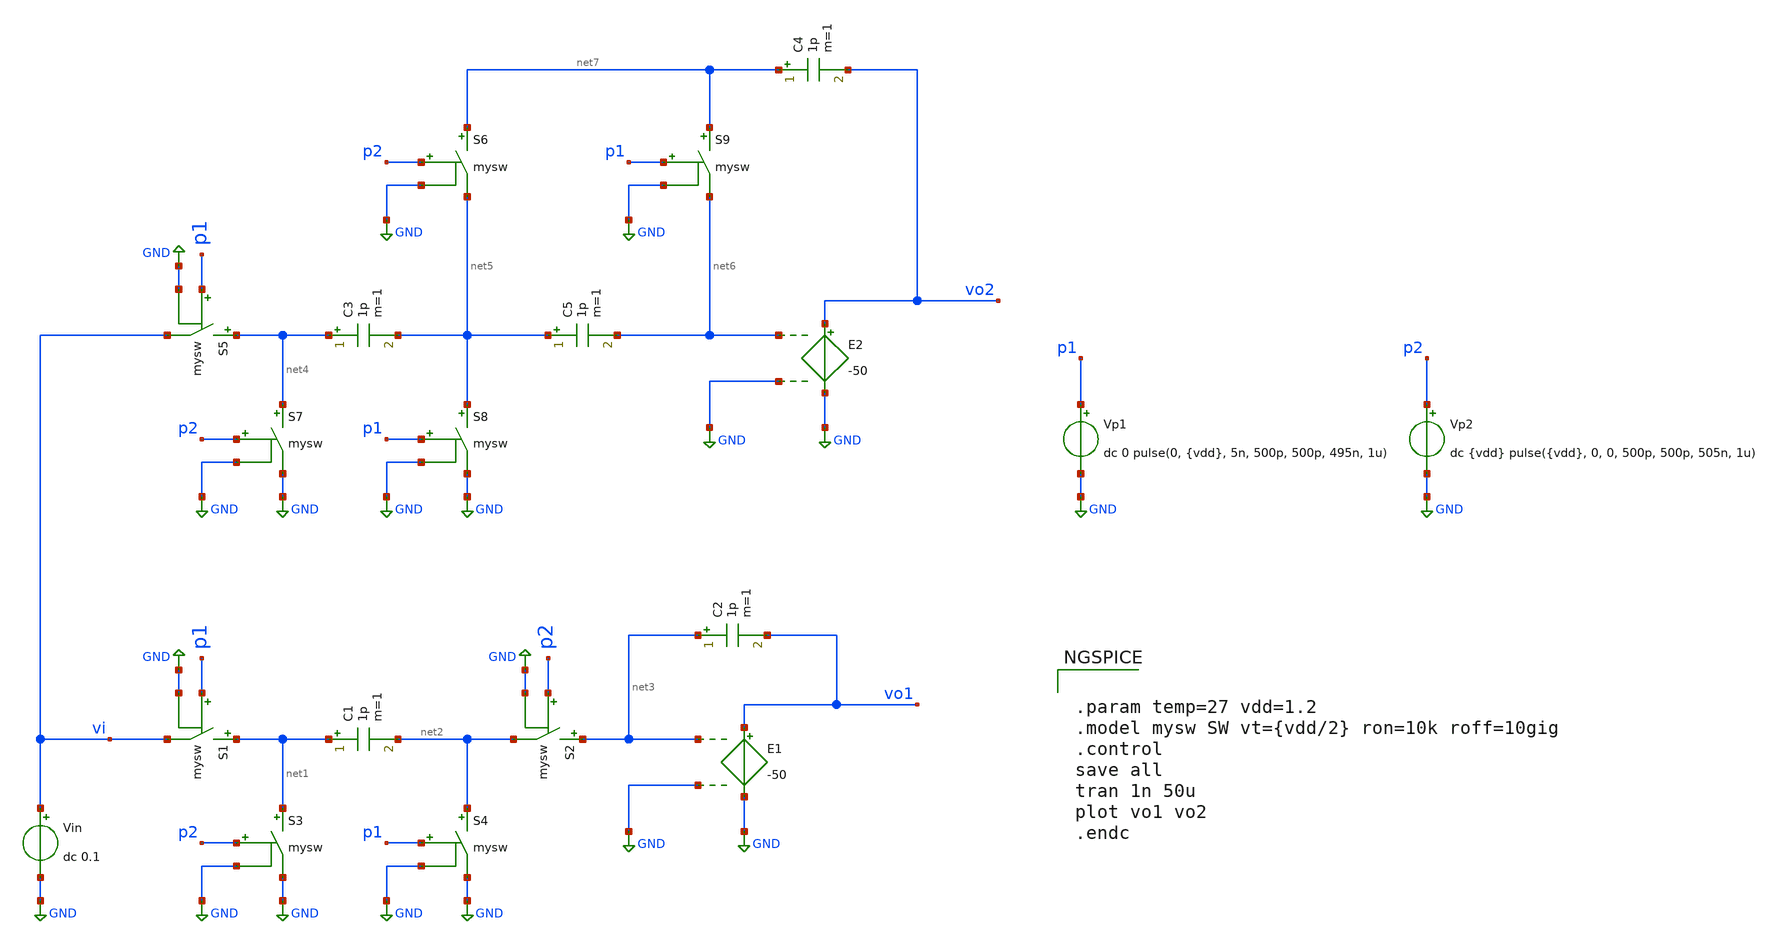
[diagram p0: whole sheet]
** sch_path: 5_Design/3_Real_circuits/sandbox_boris/tb_chae_integ.sch
**.subckt tb_chae_integ
Vp1 p1 GND dc 0 pulse(0, {vdd}, 5n, 500p, 500p, 495n, 1u)
E1 vo1 GND net3 GND -50
S1 net1 vi p1 GND mysw
Vp2 p2 GND dc {vdd} pulse({vdd}, 0, 0, 500p, 500p, 505n, 1u)
Vin vi GND dc 0.1
C1 net1 net2 1p m=1
S2 net3 net2 p2 GND mysw
C2 net3 vo1 1p m=1
S3 net1 GND p2 GND mysw
S4 net2 GND p1 GND mysw
E2 vo2 GND net6 GND -50
S5 net4 vi p1 GND mysw
C3 net4 net5 1p m=1
C4 net7 vo2 1p m=1
S7 net4 GND p2 GND mysw
S8 net5 GND p1 GND mysw
C5 net5 net6 1p m=1
S6 net7 net5 p2 GND mysw
S9 net7 net6 p1 GND mysw
**** begin user architecture code


.param temp=27 vdd=1.2
.model mysw SW vt={vdd/2} ron=10k roff=10gig
.control
save all
tran 1n 50u
plot vo1 vo2
.endc


**** end user architecture code
**.ends
.GLOBAL GND
.end
